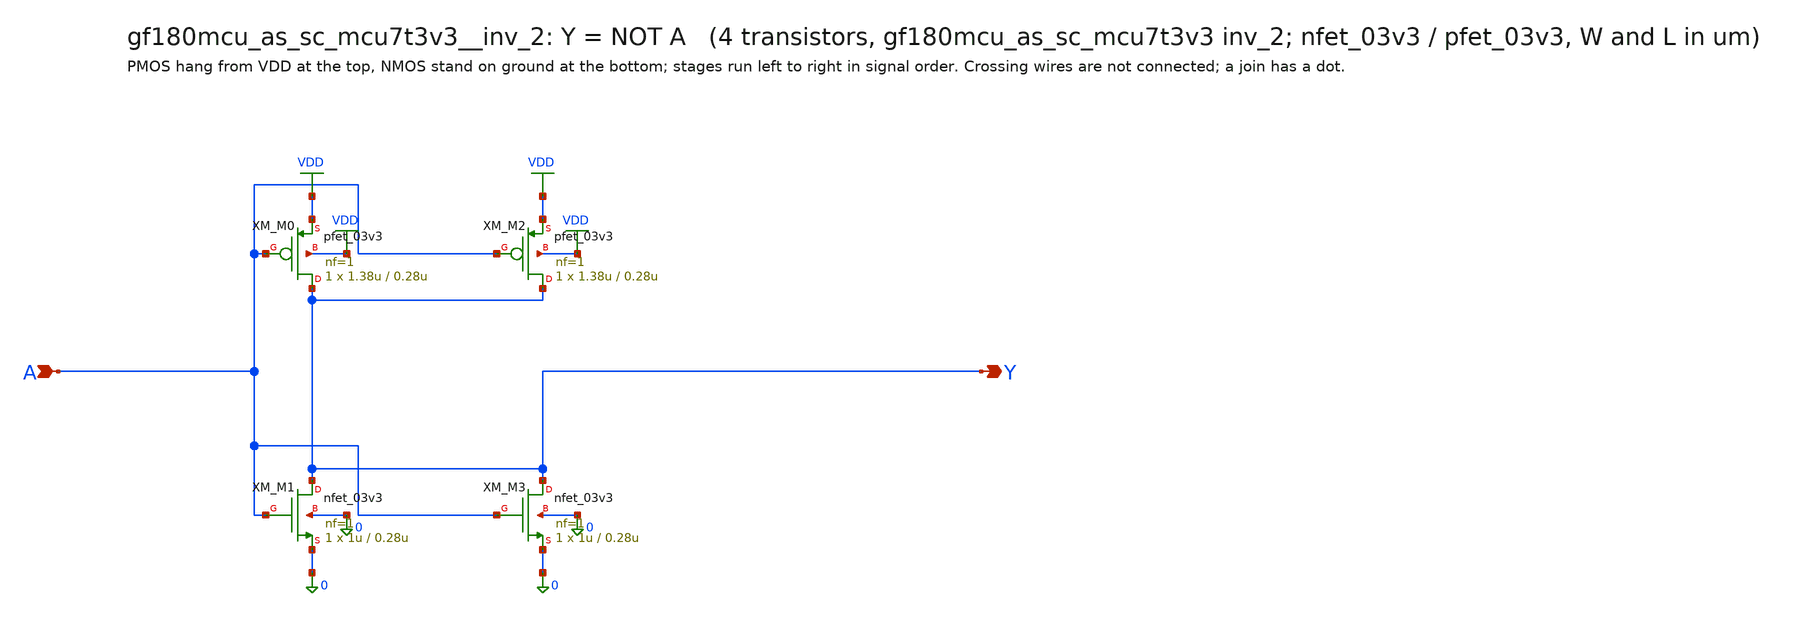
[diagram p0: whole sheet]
** sch_path: xschem/cells_tx/gf180mcu_as_sc_mcu7t3v3__inv_2.sch
**.subckt gf180mcu_as_sc_mcu7t3v3__inv_2 A Y
*.ipin A
*.opin Y
XM_M0 Y A VDD VDD pfet_03v3 L=0.28u W=1.38u nf=1 ad=6.072e-13 as=3.588e-13 pd=3.64e-06 ps=1.9e-06
+ nrd=0 nrs=0 sa=0 sb=0 sd=0 m=1
XM_M1 Y A 0 0 nfet_03v3 L=0.28u W=1u nf=1 ad=2.6e-13 as=4.4e-13 pd=1.52e-06 ps=2.88e-06 nrd=0 nrs=0
+ sa=0 sb=0 sd=0 m=1
XM_M2 Y A VDD VDD pfet_03v3 L=0.28u W=1.38u nf=1 ad=3.588e-13 as=6.072e-13 pd=1.9e-06 ps=3.64e-06
+ nrd=0 nrs=0 sa=0 sb=0 sd=0 m=1
XM_M3 Y A 0 0 nfet_03v3 L=0.28u W=1u nf=1 ad=4.4e-13 as=2.6e-13 pd=2.88e-06 ps=1.52e-06 nrd=0 nrs=0
+ sa=0 sb=0 sd=0 m=1
**.ends
.GLOBAL VDD
.end
